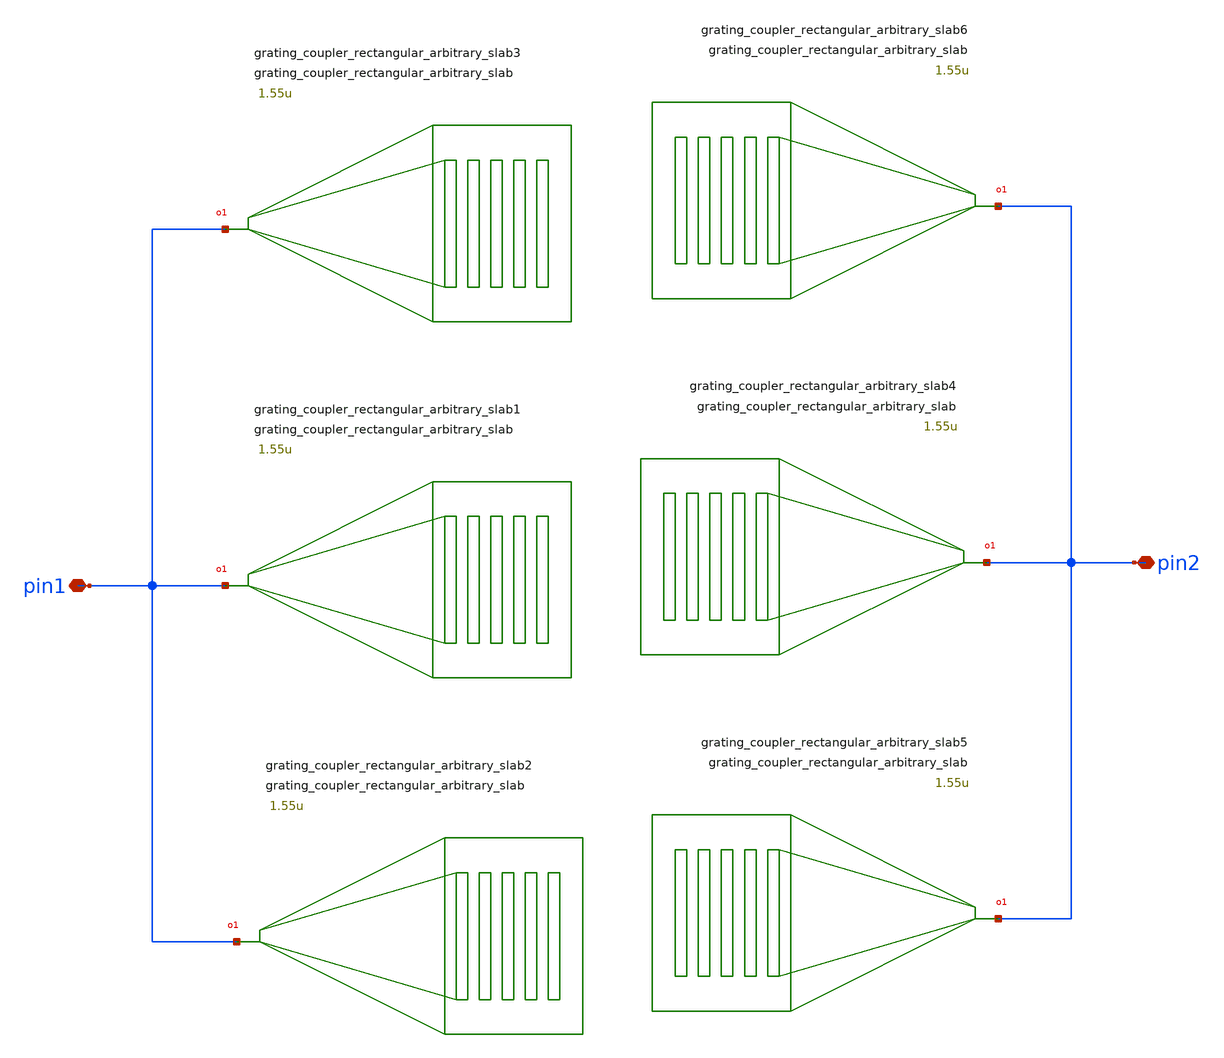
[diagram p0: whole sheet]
** sch_path: xschem/tests/test_sch/test_grating_coupler_rectangular_arbitrary_slab.sch
* Copyright (c) 2024, Mabrains LLC
* Licensed under the GNU Lesser General Public License, Version 3.0 (the "License");
* you may not use this file except in compliance with the License.
* GNU Lesser General Public License
* Version 3, 29 June 2007
* This program is free software: you can redistribute it and/or modify
* it under the terms of the GNU Lesser General Public License as published
* by the Free Software Foundation, either version 3 of the License, or
* (at your option) any later version.
* This program is distributed in the hope that it will be useful,
* but WITHOUT ANY WARRANTY; without even the implied warranty of
* MERCHANTABILITY or FITNESS FOR A PARTICULAR PURPOSE.  See the
* GNU Lesser General Public License for more details.
* You should have received a copy of the GNU Lesser General Public License
* along with this program.  If not, see <https://www.gnu.org/licenses/>.
* SPDX-License-Identifier: LGPL-3.0
**.subckt test_grating_coupler_rectangular_arbitrary_slab pin1 pin2
*.iopin pin1
*.iopin pin2
Pgrating_coupler_rectangular_arbitrary_slab1 pin1 grating_coupler_rectangular_arbitrary_slab
+ gaps=[0.2u, 0.2u, 0.2u, 0.2u, 0.2u, 0.2u, 0.2u, 0.2u, 0.2u, 0.2u] widths=[0.5u, 0.5u, 0.5u, 0.5u, 0.5u, 0.5u,
+ 0.5u, 0.5u, 0.5u, 0.5u] width_grating=11.0u length_taper=150.0u wavelength=1.55u slab_offset=2.0u
+ fiber_angle=15
Pgrating_coupler_rectangular_arbitrary_slab2 pin1 grating_coupler_rectangular_arbitrary_slab
+ gaps=[0.2u, 0.2u, 0.2u, 0.2u, 0.2u, 0.2u, 0.2u, 0.2u, 0.2u, 0.2u] widths=[0.5u, 0.5u, 0.5u, 0.5u, 0.5u, 0.5u,
+ 0.5u, 0.5u, 0.5u, 0.5u] width_grating=11.0u length_taper=150.0u wavelength=1.55u slab_offset=2.0u
+ fiber_angle=15
Pgrating_coupler_rectangular_arbitrary_slab3 pin1 grating_coupler_rectangular_arbitrary_slab
+ gaps=[0.2u, 0.2u, 0.2u, 0.2u, 0.2u, 0.2u, 0.2u, 0.2u, 0.2u, 0.2u] widths=[0.5u, 0.5u, 0.5u, 0.5u, 0.5u, 0.5u,
+ 0.5u, 0.5u, 0.5u, 0.5u] width_grating=11.0u length_taper=150.0u wavelength=1.55u slab_offset=2.0u
+ fiber_angle=15
Pgrating_coupler_rectangular_arbitrary_slab4 pin2 grating_coupler_rectangular_arbitrary_slab
+ gaps=[0.2u, 0.2u, 0.2u, 0.2u, 0.2u, 0.2u, 0.2u, 0.2u, 0.2u, 0.2u] widths=[0.5u, 0.5u, 0.5u, 0.5u, 0.5u, 0.5u,
+ 0.5u, 0.5u, 0.5u, 0.5u] width_grating=11.0u length_taper=150.0u wavelength=1.55u slab_offset=2.0u
+ fiber_angle=15
Pgrating_coupler_rectangular_arbitrary_slab5 pin2 grating_coupler_rectangular_arbitrary_slab
+ gaps=[0.2u, 0.2u, 0.2u, 0.2u, 0.2u, 0.2u, 0.2u, 0.2u, 0.2u, 0.2u] widths=[0.5u, 0.5u, 0.5u, 0.5u, 0.5u, 0.5u,
+ 0.5u, 0.5u, 0.5u, 0.5u] width_grating=11.0u length_taper=150.0u wavelength=1.55u slab_offset=2.0u
+ fiber_angle=15
Pgrating_coupler_rectangular_arbitrary_slab6 pin2 grating_coupler_rectangular_arbitrary_slab
+ gaps=[0.2u, 0.2u, 0.2u, 0.2u, 0.2u, 0.2u, 0.2u, 0.2u, 0.2u, 0.2u] widths=[0.5u, 0.5u, 0.5u, 0.5u, 0.5u, 0.5u,
+ 0.5u, 0.5u, 0.5u, 0.5u] width_grating=11.0u length_taper=150.0u wavelength=1.55u slab_offset=2.0u
+ fiber_angle=15
**.ends
.end
